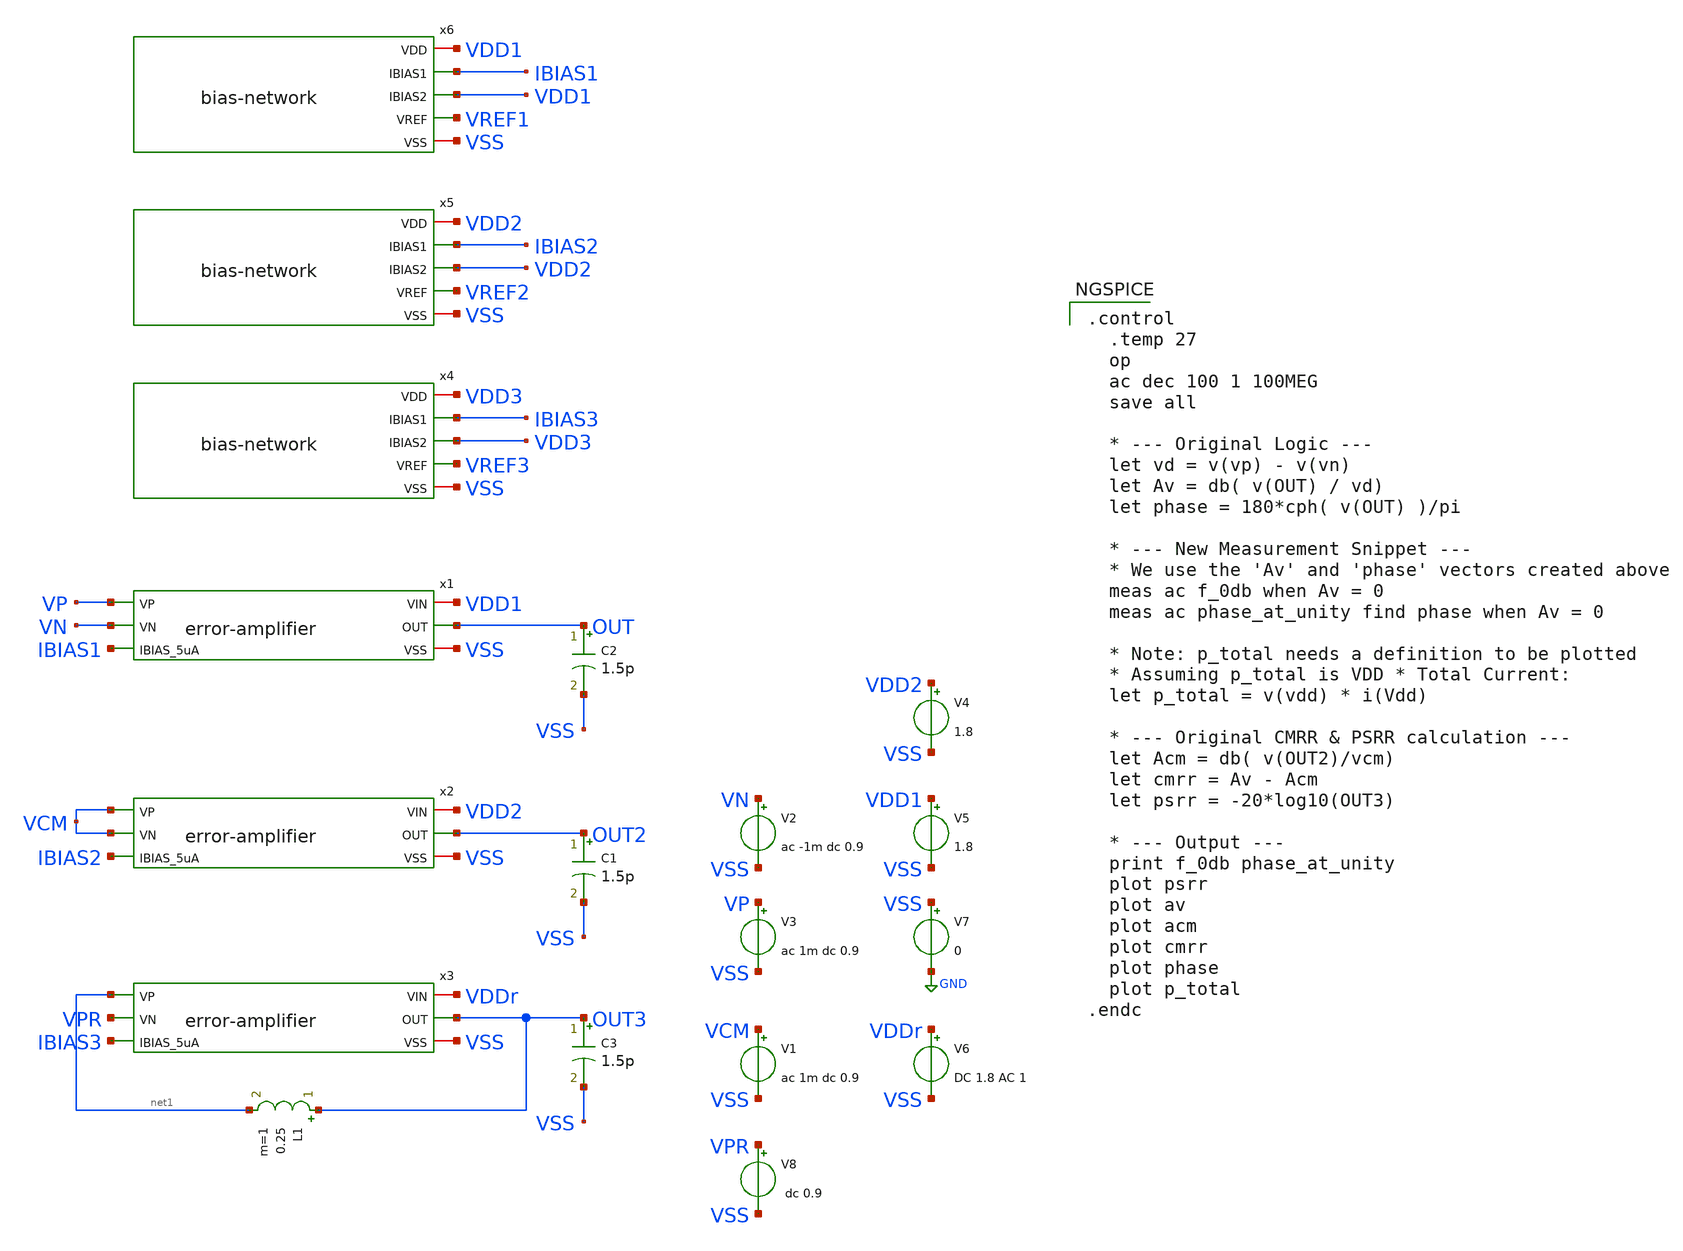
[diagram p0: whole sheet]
** sch_path: xschem/error-amplifier/testbench/tb_ac.sch
**.subckt tb_ac
V2 VN VSS ac -1m dc 0.9
V3 VP VSS ac 1m dc 0.9
V5 VDD1 VSS 1.8
V7 VSS GND 0
C2 OUT VSS 1.5p m=1
C1 OUT2 VSS 1.5p m=1
V1 VCM VSS ac 1m dc 0.9
V4 VDD2 VSS 1.8
C3 OUT3 VSS 1.5p m=1
V6 VDDr VSS DC 1.8 AC 1
L1 OUT3 net1 0.25 m=1
V8 VPR VSS dc 0.9
x1 VDD1 VP VN IBIAS1 OUT VSS error-amplifier
x2 VDD2 VCM VCM IBIAS2 OUT2 VSS error-amplifier
x3 VDDr net1 VPR IBIAS3 OUT3 VSS error-amplifier
x4 VDD3 IBIAS3 VDD3 VREF3 VSS bias-network
x5 VDD2 IBIAS2 VDD2 VREF2 VSS bias-network
x6 VDD1 IBIAS1 VDD1 VREF1 VSS bias-network
**** begin user architecture code

.control
  .temp 27
  op
  ac dec 100 1 100MEG
  save all

  * --- Original Logic ---
  let vd = v(vp) - v(vn)
  let Av = db( v(OUT) / vd)
  let phase = 180*cph( v(OUT) )/pi

  * --- New Measurement Snippet ---
  * We use the 'Av' and 'phase' vectors created above
  meas ac f_0db when Av = 0
  meas ac phase_at_unity find phase when Av = 0

  * Note: p_total needs a definition to be plotted
  * Assuming p_total is VDD * Total Current:
  let p_total = v(vdd) * i(Vdd)

  * --- Original CMRR & PSRR calculation ---
  let Acm = db( v(OUT2)/vcm)
  let cmrr = Av - Acm
  let psrr = -20*log10(OUT3)

  * --- Output ---
  print f_0db phase_at_unity
  plot psrr
  plot av
  plot acm
  plot cmrr
  plot phase
  plot p_total
.endc




** opencircuitdesign pdks install
.lib $::SKYWATER_MODELS/sky130.lib.spice ss


**** end user architecture code
**.ends

* expanding   symbol:
*+  /foss/designs/2026/tt_sky26b_ldo_andriansyah/xschem/error-amplifier/error-amplifier.sym # of pins=6
** sym_path: xschem/error-amplifier/error-amplifier.sym
** sch_path: xschem/error-amplifier/error-amplifier.sch
.subckt error-amplifier VIN VP VN IBIAS_5uA OUT VSS
*.ipin IBIAS_5uA
*.ipin VN
*.ipin VP
*.iopin VIN
*.iopin VSS
*.opin OUT
XM1 net2 net2 VSS VSS sky130_fd_pr__nfet_01v8 L=0.6 W=4.2 nf=4 ad='int((nf+1)/2) * W/nf * 0.29' as='int((nf+2)/2) * W/nf * 0.29'
+ pd='2*int((nf+1)/2) * (W/nf + 0.29)' ps='2*int((nf+2)/2) * (W/nf + 0.29)' nrd='0.29 / W' nrs='0.29 / W'
+ sa=0 sb=0 sd=0 mult=1 m=1
XM2 OUT net2 VSS VSS sky130_fd_pr__nfet_01v8 L=0.6 W=4.2 nf=4 ad='int((nf+1)/2) * W/nf * 0.29' as='int((nf+2)/2) * W/nf * 0.29'
+ pd='2*int((nf+1)/2) * (W/nf + 0.29)' ps='2*int((nf+2)/2) * (W/nf + 0.29)' nrd='0.29 / W' nrs='0.29 / W'
+ sa=0 sb=0 sd=0 mult=1 m=1
XM3 net2 VN net1 VDD sky130_fd_pr__pfet_01v8 L=0.6 W=14 nf=4 ad='int((nf+1)/2) * W/nf * 0.29' as='int((nf+2)/2) * W/nf * 0.29'
+ pd='2*int((nf+1)/2) * (W/nf + 0.29)' ps='2*int((nf+2)/2) * (W/nf + 0.29)' nrd='0.29 / W' nrs='0.29 / W'
+ sa=0 sb=0 sd=0 mult=2 m=2
XM4 OUT VP net1 VDD sky130_fd_pr__pfet_01v8 L=0.6 W=14 nf=4 ad='int((nf+1)/2) * W/nf * 0.29' as='int((nf+2)/2) * W/nf * 0.29'
+ pd='2*int((nf+1)/2) * (W/nf + 0.29)' ps='2*int((nf+2)/2) * (W/nf + 0.29)' nrd='0.29 / W' nrs='0.29 / W'
+ sa=0 sb=0 sd=0 mult=2 m=2
XM5 net1 IBIAS_5uA VIN VIN sky130_fd_pr__pfet_01v8 L=0.6 W=6.6 nf=4 ad='int((nf+1)/2) * W/nf * 0.29'
+ as='int((nf+2)/2) * W/nf * 0.29' pd='2*int((nf+1)/2) * (W/nf + 0.29)' ps='2*int((nf+2)/2) * (W/nf + 0.29)'
+ nrd='0.29 / W' nrs='0.29 / W' sa=0 sb=0 sd=0 mult=1 m=1
XM6 IBIAS_5uA IBIAS_5uA VIN VIN sky130_fd_pr__pfet_01v8 L=0.6 W=6.6 nf=4 ad='int((nf+1)/2) * W/nf * 0.29'
+ as='int((nf+2)/2) * W/nf * 0.29' pd='2*int((nf+1)/2) * (W/nf + 0.29)' ps='2*int((nf+2)/2) * (W/nf + 0.29)'
+ nrd='0.29 / W' nrs='0.29 / W' sa=0 sb=0 sd=0 mult=1 m=1
.ends


* expanding   symbol:
*+  /foss/designs/2026/tt_sky26b_ldo_andriansyah/xschem/bias-net/schematics/bias-network.sym # of pins=5
** sym_path: xschem/bias-net/schematics/bias-network.sym
** sch_path: xschem/bias-net/schematics/bias-network.sch
.subckt bias-network VDD IBIAS1 IBIAS2 VREF VSS
*.iopin VDD
*.iopin VSS
*.opin IBIAS1
*.opin IBIAS2
*.opin VREF
XM2 VREF VREF VSS VSS sky130_fd_pr__nfet_01v8 L=2 W=3 nf=4 ad='int((nf+1)/2) * W/nf * 0.29' as='int((nf+2)/2) * W/nf * 0.29'
+ pd='2*int((nf+1)/2) * (W/nf + 0.29)' ps='2*int((nf+2)/2) * (W/nf + 0.29)' nrd='0.29 / W' nrs='0.29 / W'
+ sa=0 sb=0 sd=0 mult=2 m=2
XR1 VREF net1 VSS sky130_fd_pr__res_xhigh_po_0p69 L=6.9 mult=1 m=1
XR2 net2 net1 VSS sky130_fd_pr__res_xhigh_po_0p69 L=6.9 mult=1 m=1
XR3 net2 net3 VSS sky130_fd_pr__res_xhigh_po_0p69 L=6.9 mult=1 m=1
XR4 net4 net3 VSS sky130_fd_pr__res_xhigh_po_0p69 L=6.9 mult=1 m=1
XR5 net4 net5 VSS sky130_fd_pr__res_xhigh_po_0p69 L=6.9 mult=1 m=1
XR6 net9 net10 VSS sky130_fd_pr__res_xhigh_po_0p69 L=6.9 mult=1 m=1
XR7 net9 net8 VSS sky130_fd_pr__res_xhigh_po_0p69 L=6.9 mult=1 m=1
XR8 net7 net8 VSS sky130_fd_pr__res_xhigh_po_0p69 L=6.9 mult=1 m=1
XR9 net7 net6 VSS sky130_fd_pr__res_xhigh_po_0p69 L=6.9 mult=1 m=1
XR10 net5 net6 VSS sky130_fd_pr__res_xhigh_po_0p69 L=6.9 mult=1 m=1
XM1 IBIAS1 VREF VSS VSS sky130_fd_pr__nfet_01v8 L=2 W=3 nf=4 ad='int((nf+1)/2) * W/nf * 0.29' as='int((nf+2)/2) * W/nf * 0.29'
+ pd='2*int((nf+1)/2) * (W/nf + 0.29)' ps='2*int((nf+2)/2) * (W/nf + 0.29)' nrd='0.29 / W' nrs='0.29 / W'
+ sa=0 sb=0 sd=0 mult=2 m=2
XM3 IBIAS2 VREF VSS VSS sky130_fd_pr__nfet_01v8 L=2 W=3 nf=4 ad='int((nf+1)/2) * W/nf * 0.29' as='int((nf+2)/2) * W/nf * 0.29'
+ pd='2*int((nf+1)/2) * (W/nf + 0.29)' ps='2*int((nf+2)/2) * (W/nf + 0.29)' nrd='0.29 / W' nrs='0.29 / W'
+ sa=0 sb=0 sd=0 mult=2 m=2
XR11 net10 net11 VSS sky130_fd_pr__res_xhigh_po_0p69 L=6.9 mult=1 m=1
XR12 net12 net11 VSS sky130_fd_pr__res_xhigh_po_0p69 L=6.9 mult=1 m=1
XR13 net12 net13 VSS sky130_fd_pr__res_xhigh_po_0p69 L=6.9 mult=1 m=1
XR14 net14 net13 VSS sky130_fd_pr__res_xhigh_po_0p69 L=6.9 mult=1 m=1
XR15 net14 net15 VSS sky130_fd_pr__res_xhigh_po_0p69 L=6.9 mult=1 m=1
XR16 net19 VDD VSS sky130_fd_pr__res_xhigh_po_0p69 L=6.9 mult=1 m=1
XR17 net19 net18 VSS sky130_fd_pr__res_xhigh_po_0p69 L=6.9 mult=1 m=1
XR18 net17 net18 VSS sky130_fd_pr__res_xhigh_po_0p69 L=6.9 mult=1 m=1
XR19 net17 net16 VSS sky130_fd_pr__res_xhigh_po_0p69 L=6.9 mult=1 m=1
XR20 net15 net16 VSS sky130_fd_pr__res_xhigh_po_0p69 L=6.9 mult=1 m=1
XR21 VSS VSS VSS sky130_fd_pr__res_xhigh_po_0p69 L=6.9 mult=1 m=1
XR22 VSS VSS VSS sky130_fd_pr__res_xhigh_po_0p69 L=6.9 mult=1 m=1
.ends

.GLOBAL GND
.end
